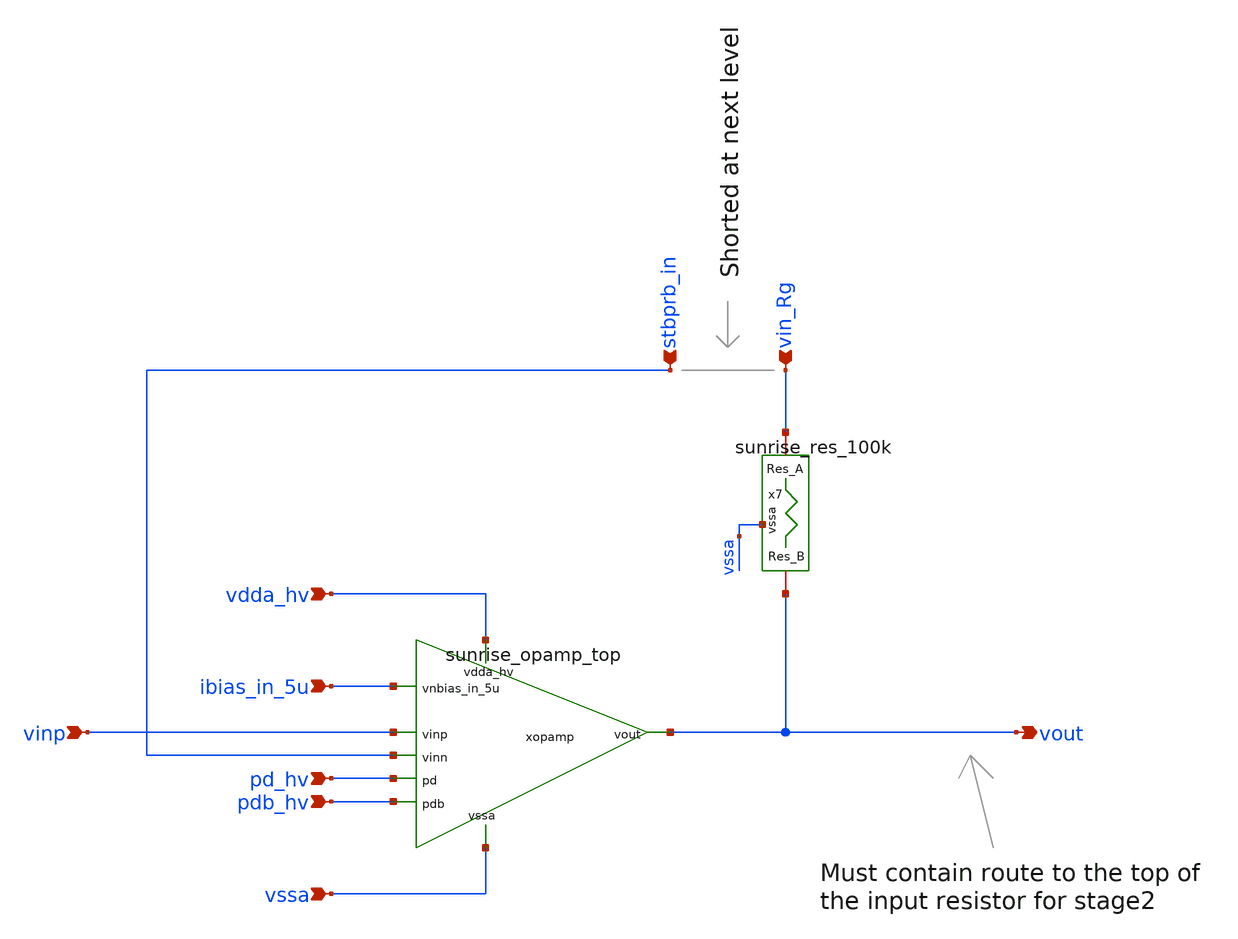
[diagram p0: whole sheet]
** sch_path: Schematics_Layout/sunrise_IA_loop/sunrise_IA_loop.sch
**.subckt sunrise_IA_loop vinp vin_Rg pd_hv pdb_hv vout stbprb_in ibias_in_5u vdda_hv vssa
*.ipin vinp
*.ipin vin_Rg
*.ipin pd_hv
*.ipin pdb_hv
*.opin vout
*.ipin stbprb_in
*.ipin ibias_in_5u
*.ipin vdda_hv
*.ipin vssa
x7 vssa vout vin_Rg sunrise_res_100k
xopamp vdda_hv ibias_in_5u vout vinp stbprb_in pd_hv pdb_hv vssa sunrise_opamp_top
**.ends
.end
